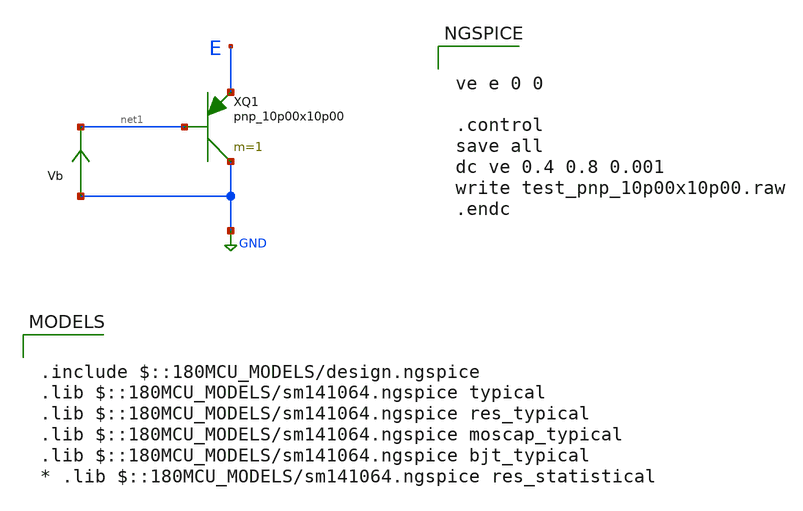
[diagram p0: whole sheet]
** sch_path: gf180mcuD/xschem_libs/gf180mcu_tests/test_pnp_10p00x10p00/schematic/test_pnp_10p00x10p00.sch
* Copyright 2022 GlobalFoundries PDK Authors
* Licensed under the Apache License, Version 2.0 (the "License");
* you may not use this file except in compliance with the License.
* You may obtain a copy of the License at
* https://www.apache.org/licenses/LICENSE-2.0
* Unless required by applicable law or agreed to in writing, software
* distributed under the License is distributed on an "AS IS" BASIS,
* WITHOUT WARRANTIES OR CONDITIONS OF ANY KIND, either express or implied.
* See the License for the specific language governing permissions and
* limitations under the License.
**.subckt test_pnp_10p00x10p00
XQ1 GND net1 E pnp_10p00x10p00 m=1
Vb GND net1 0
.save i(vb)
**** begin user architecture code

.include $::180MCU_MODELS/design.ngspice
.lib $::180MCU_MODELS/sm141064.ngspice typical
.lib $::180MCU_MODELS/sm141064.ngspice res_typical
.lib $::180MCU_MODELS/sm141064.ngspice moscap_typical
.lib $::180MCU_MODELS/sm141064.ngspice bjt_typical
* .lib $::180MCU_MODELS/sm141064.ngspice res_statistical



ve e 0 0

.control
save all
dc ve 0.4 0.8 0.001
write test_pnp_10p00x10p00.raw
.endc


**** end user architecture code
**.ends
.GLOBAL GND
.end
